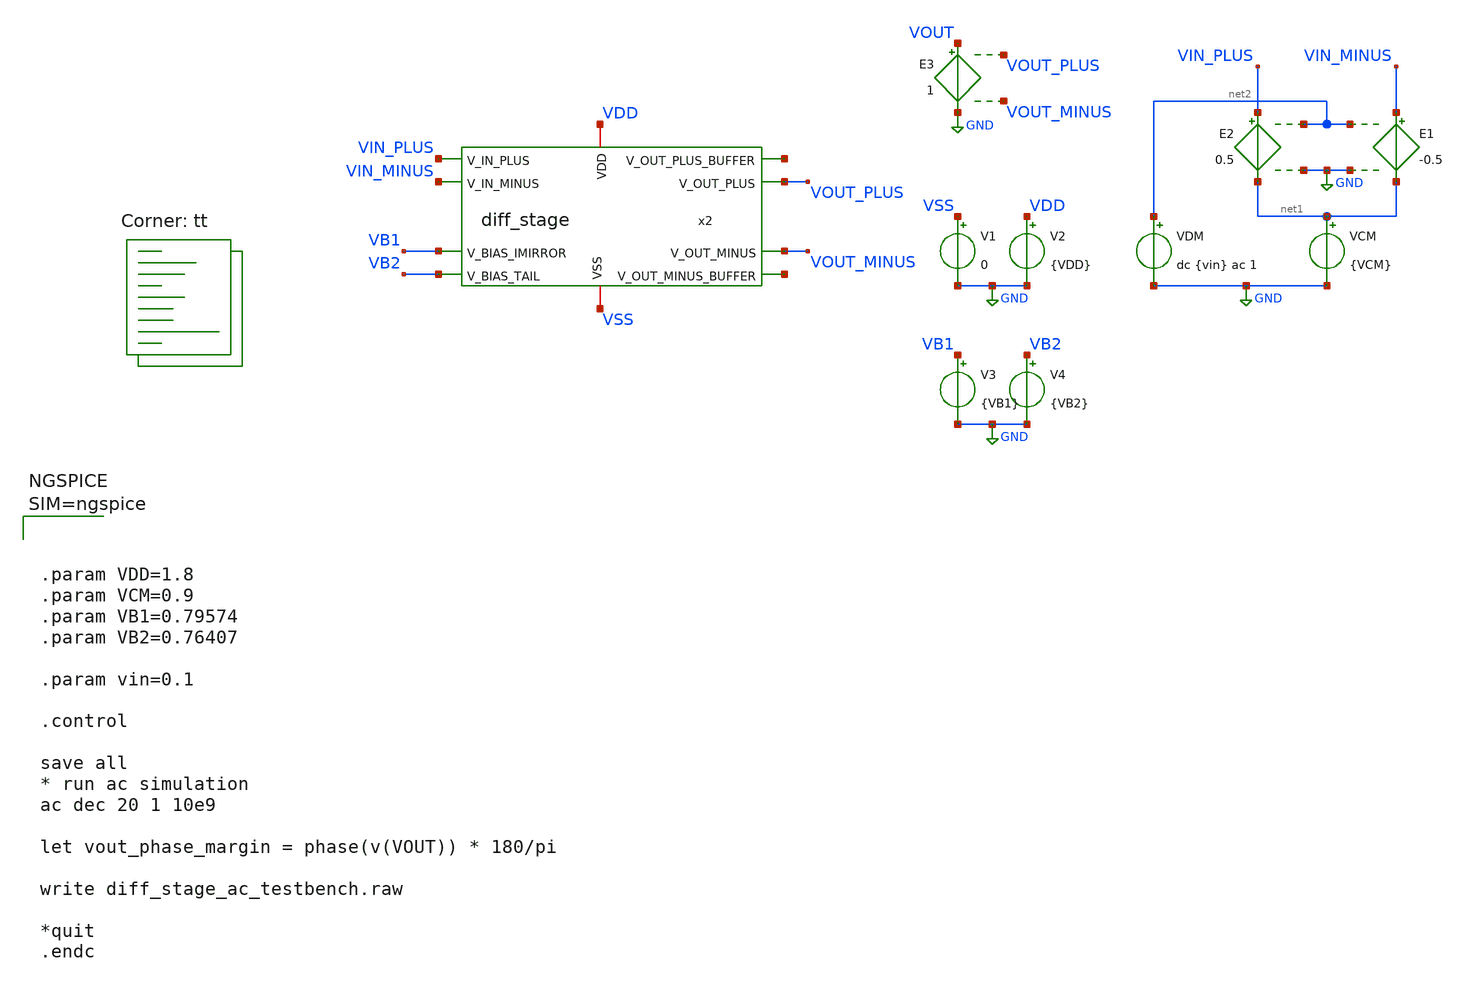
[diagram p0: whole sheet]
** sch_path: xschem/diff_stage_ac_testbench.sch
**.subckt diff_stage_ac_testbench
x2 VDD VSS VOUT_MINUS VOUT_PLUS net3 net4 VIN_PLUS VIN_MINUS VB1 VB2 diff_stage
V1 VSS GND 0
V2 VDD GND {VDD}
VDM net2 GND dc {vin} ac 1
VCM net1 GND {VCM}
E1 VIN_MINUS net1 net2 GND -0.5
E2 VIN_PLUS net1 net2 GND 0.5
E3 VOUT GND VOUT_PLUS VOUT_MINUS 1
V3 VB1 GND {VB1}
V4 VB2 GND {VB2}
**** begin user architecture code




.param VDD=1.8
.param VCM=0.9
.param VB1=0.79574
.param VB2=0.76407

.param vin=0.1

.control

save all
* run ac simulation
ac dec 20 1 10e9

let vout_phase_margin = phase(v(VOUT)) * 180/pi

write diff_stage_ac_testbench.raw

*quit
.endc



.lib $::SKYWATER_MODELS/sky130.lib.spice tt
**** end user architecture code
**.ends

* expanding   symbol:  diff_stage.sym # of pins=10
** sym_path: xschem/diff_stage.sym
** sch_path: xschem/diff_stage.sch
.subckt diff_stage VDD VSS V_OUT_MINUS V_OUT_PLUS V_OUT_MINUS_BUFFER V_OUT_PLUS_BUFFER V_IN_PLUS
+ V_IN_MINUS V_BIAS_IMIRROR V_BIAS_TAIL
*.opin V_OUT_PLUS
*.opin V_OUT_PLUS_BUFFER
*.opin V_OUT_MINUS
*.opin V_OUT_MINUS_BUFFER
*.ipin V_BIAS_IMIRROR
*.ipin V_IN_MINUS
*.ipin V_IN_PLUS
*.ipin V_BIAS_TAIL
*.iopin VDD
*.iopin VSS
x1 VDD V_OUT_MINUS V_BIAS_IMIRROR V_OUT_PLUS V_OUT_PLUS_BUFFER V_IN_MINUS VSS V_DRAIN_TAIL
+ diff_stage_half
x2 VDD V_OUT_PLUS V_BIAS_IMIRROR V_OUT_MINUS V_OUT_MINUS_BUFFER V_IN_PLUS VSS V_DRAIN_TAIL
+ diff_stage_half
XM1 V_DRAIN_TAIL V_BIAS_TAIL VSS VSS sky130_fd_pr__nfet_01v8 L=2 W=4 nf=2 ad='int((nf+1)/2) * W/nf * 0.29'
+ as='int((nf+2)/2) * W/nf * 0.29' pd='2*int((nf+1)/2) * (W/nf + 0.29)' ps='2*int((nf+2)/2) * (W/nf + 0.29)'
+ nrd='0.29 / W' nrs='0.29 / W' sa=0 sb=0 sd=0 mult=1 m=1
.ends


* expanding   symbol:  diff_stage_half.sym # of pins=8
** sym_path: xschem/diff_stage_half.sym
** sch_path: xschem/diff_stage_half.sch
.subckt diff_stage_half VDD V_FB_CROSSCOUPLED V_BIAS_IMIRROR V_OUT_DIFF V_OUT_DIFF_BUFFER V_IN_RING
+ VSS V_DRAIN_TAIL
*.ipin V_BIAS_IMIRROR
*.ipin V_FB_CROSSCOUPLED
*.ipin V_IN_RING
*.opin V_OUT_DIFF
*.iopin VDD
*.iopin VSS
*.opin V_OUT_DIFF_BUFFER
*.iopin V_DRAIN_TAIL
XM1 V_OUT_DIFF V_BIAS_IMIRROR VDD VDD sky130_fd_pr__pfet_01v8 L=2 W=4 nf=2 ad='int((nf+1)/2) * W/nf * 0.29'
+ as='int((nf+2)/2) * W/nf * 0.29' pd='2*int((nf+1)/2) * (W/nf + 0.29)' ps='2*int((nf+2)/2) * (W/nf + 0.29)'
+ nrd='0.29 / W' nrs='0.29 / W' sa=0 sb=0 sd=0 mult=1 m=1
XM2 V_OUT_DIFF V_FB_CROSSCOUPLED VDD VDD sky130_fd_pr__pfet_01v8 L=2 W=4 nf=2 ad='int((nf+1)/2) * W/nf * 0.29'
+ as='int((nf+2)/2) * W/nf * 0.29' pd='2*int((nf+1)/2) * (W/nf + 0.29)' ps='2*int((nf+2)/2) * (W/nf + 0.29)'
+ nrd='0.29 / W' nrs='0.29 / W' sa=0 sb=0 sd=0 mult=1 m=1
XM3 V_OUT_DIFF V_IN_RING V_DRAIN_TAIL VSS sky130_fd_pr__nfet_01v8 L=2 W=4 nf=2 ad='int((nf+1)/2) * W/nf * 0.29'
+ as='int((nf+2)/2) * W/nf * 0.29' pd='2*int((nf+1)/2) * (W/nf + 0.29)' ps='2*int((nf+2)/2) * (W/nf + 0.29)'
+ nrd='0.29 / W' nrs='0.29 / W' sa=0 sb=0 sd=0 mult=1 m=1
XM4 VSS V_OUT_DIFF VSS VSS sky130_fd_pr__nfet_01v8 L=11 W=11 nf=1 ad='int((nf+1)/2) * W/nf * 0.29' as='int((nf+2)/2) * W/nf * 0.29'
+ pd='2*int((nf+1)/2) * (W/nf + 0.29)' ps='2*int((nf+2)/2) * (W/nf + 0.29)' nrd='0.29 / W' nrs='0.29 / W'
+ sa=0 sb=0 sd=0 mult=1 m=1
x1 VDD VSS V_OUT_DIFF_BUFFER V_OUT_DIFF min_buffer
.ends


* expanding   symbol:  min_buffer.sym # of pins=4
** sym_path: xschem/min_buffer.sym
** sch_path: xschem/min_buffer.sch
.subckt min_buffer VDD VSS VOUT_BUFFER VIN_BUFFER
*.ipin VIN_BUFFER
*.opin VOUT_BUFFER
*.iopin VDD
*.iopin VSS
x1 VDD VSS VOUT_BUFFER INT_BUFFER min_inv
x2 VDD VSS INT_BUFFER VIN_BUFFER min_inv
.ends


* expanding   symbol:  min_inv.sym # of pins=4
** sym_path: xschem/min_inv.sym
** sch_path: xschem/min_inv.sch
.subckt min_inv VDD VSS VOUT_INV VIN_INV
*.iopin VDD
*.iopin VSS
*.ipin VIN_INV
*.opin VOUT_INV
XM2 VOUT_INV VIN_INV VSS VSS sky130_fd_pr__nfet_01v8 L=0.15 W=1 nf=1 ad='int((nf+1)/2) * W/nf * 0.29'
+ as='int((nf+2)/2) * W/nf * 0.29' pd='2*int((nf+1)/2) * (W/nf + 0.29)' ps='2*int((nf+2)/2) * (W/nf + 0.29)'
+ nrd='0.29 / W' nrs='0.29 / W' sa=0 sb=0 sd=0 mult=1 m=1
XM3 VOUT_INV VIN_INV VDD VDD sky130_fd_pr__pfet_01v8 L=0.15 W=1 nf=1 ad='int((nf+1)/2) * W/nf * 0.29'
+ as='int((nf+2)/2) * W/nf * 0.29' pd='2*int((nf+1)/2) * (W/nf + 0.29)' ps='2*int((nf+2)/2) * (W/nf + 0.29)'
+ nrd='0.29 / W' nrs='0.29 / W' sa=0 sb=0 sd=0 mult=1 m=1
.ends

.GLOBAL GND
.end
